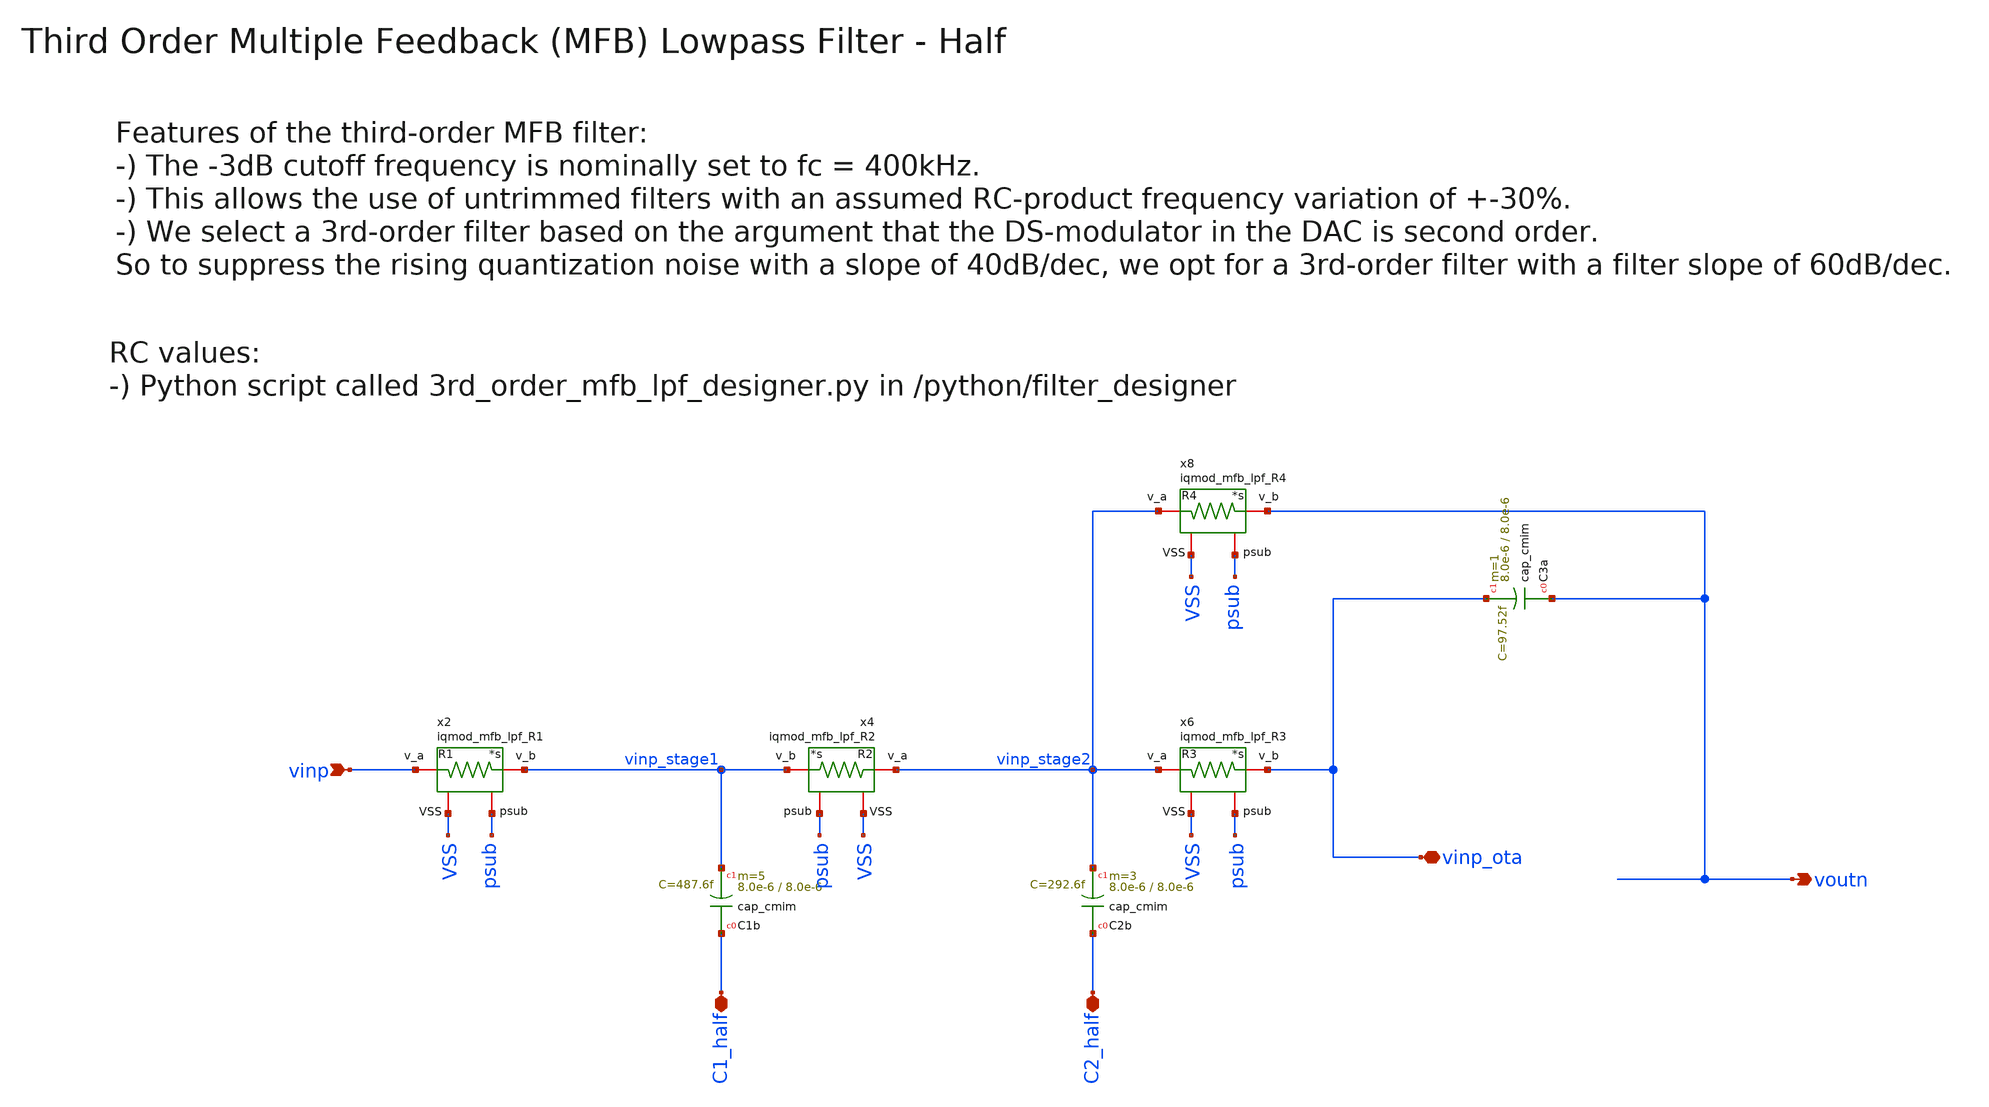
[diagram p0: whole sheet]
** sch_path: ihp130/macros/iqmod/schematic/iqmod_mfb_lpf_half.sch
**.subckt iqmod_mfb_lpf_half vinp voutn C1_half C2_half vinp_ota
*.ipin vinp
*.opin voutn
*.iopin C1_half
*.iopin C2_half
*.iopin vinp_ota
XC1b C1_half vinp_stage1 cap_cmim w=8.0e-6 l=8.0e-6 m=5 mm_ok=1
XC2b C2_half vinp_stage2 cap_cmim w=8.0e-6 l=8.0e-6 m=3 mm_ok=1
XC3a voutn vinp_ota cap_cmim w=8.0e-6 l=8.0e-6 m=1 mm_ok=1
x2 psub vinp_stage1 vinp VSS iqmod_mfb_lpf_R1
x4 vinp_stage1 vinp_stage2 psub VSS iqmod_mfb_lpf_R2
x6 vinp_ota vinp_stage2 psub VSS iqmod_mfb_lpf_R3
x8 voutn vinp_stage2 psub VSS iqmod_mfb_lpf_R4
**.ends
.end
